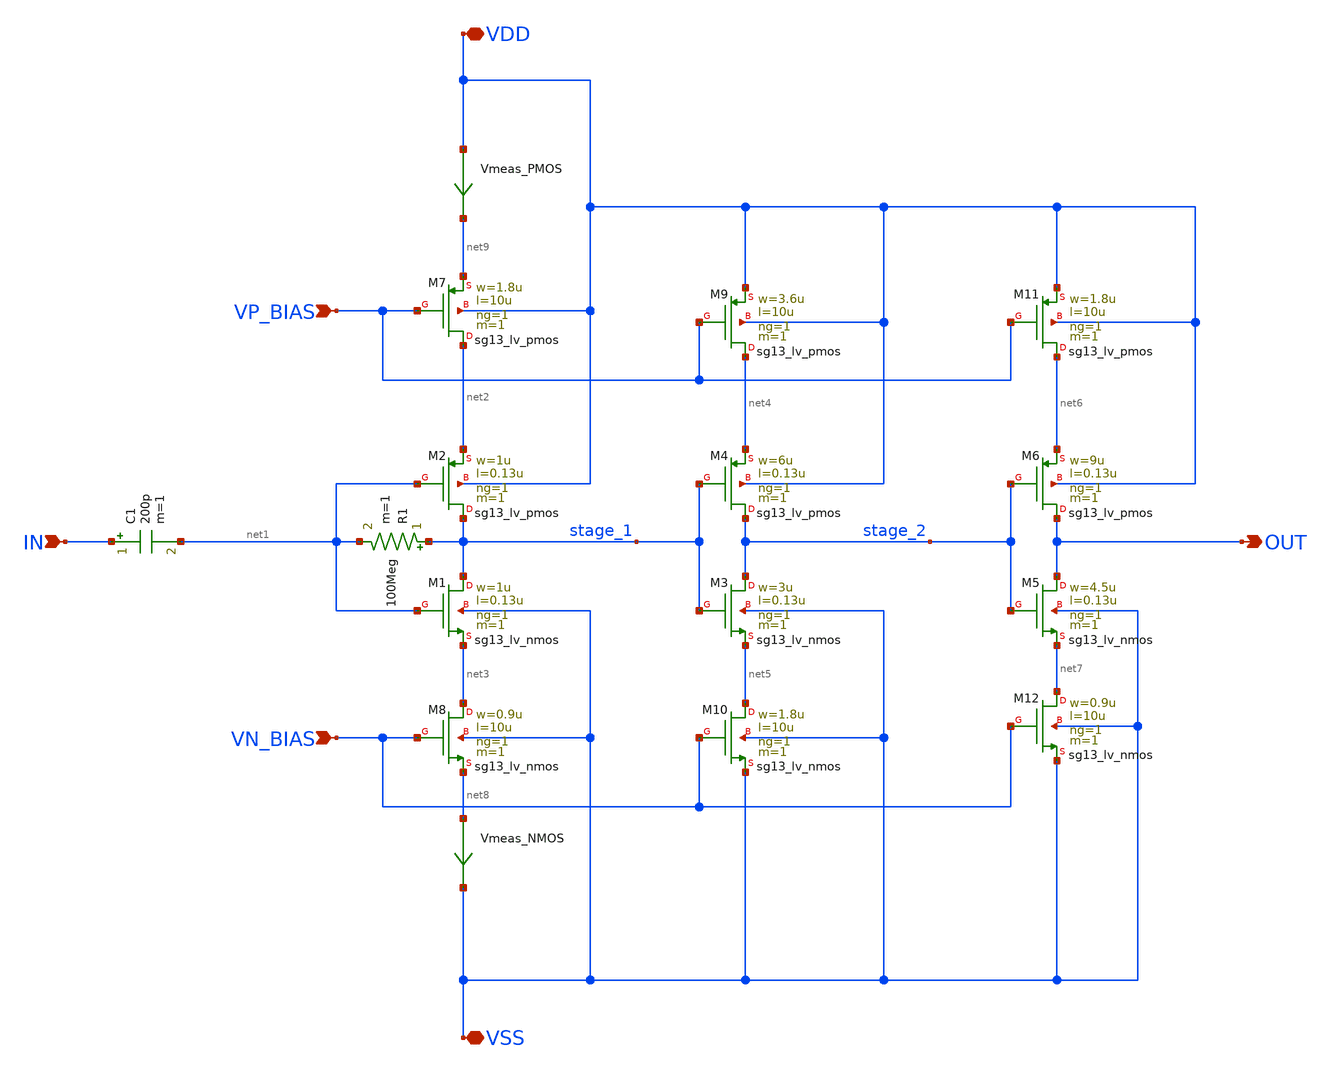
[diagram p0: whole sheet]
** sch_path: clock_gen.sch
**.subckt clock_gen VSS VDD IN OUT VP_BIAS VN_BIAS
*.iopin VSS
*.iopin VDD
*.ipin IN
*.opin OUT
*.ipin VP_BIAS
*.ipin VN_BIAS
XM1 stage_1 net1 net3 VSS sg13_lv_nmos w=1u l=0.13u ng=1 m=1 mm_ok=1
XM2 stage_1 net1 net2 VDD sg13_lv_pmos w=1u l=0.13u ng=1 m=1 mm_ok=1
R1 stage_1 net1 100Meg m=1
C1 IN net1 200p m=1
XM3 stage_2 stage_1 net5 VSS sg13_lv_nmos w=3u l=0.13u ng=1 m=1 mm_ok=1
XM4 stage_2 stage_1 net4 VDD sg13_lv_pmos w=6u l=0.13u ng=1 m=1 mm_ok=1
XM5 OUT stage_2 net7 VSS sg13_lv_nmos w=4.5u l=0.13u ng=1 m=1 mm_ok=1
XM6 OUT stage_2 net6 VDD sg13_lv_pmos w=9u l=0.13u ng=1 m=1 mm_ok=1
XM7 net2 VP_BIAS net9 VDD sg13_lv_pmos w=1.8u l=10u ng=1 m=1 mm_ok=1
XM8 net3 VN_BIAS net8 VSS sg13_lv_nmos w=0.9u l=10u ng=1 m=1 mm_ok=1
XM9 net4 VP_BIAS VDD VDD sg13_lv_pmos w=3.6u l=10u ng=1 m=1 mm_ok=1
XM10 net5 VN_BIAS VSS VSS sg13_lv_nmos w=1.8u l=10u ng=1 m=1 mm_ok=1
XM11 net6 VP_BIAS VDD VDD sg13_lv_pmos w=1.8u l=10u ng=1 m=1 mm_ok=1
XM12 net7 VN_BIAS VSS VSS sg13_lv_nmos w=0.9u l=10u ng=1 m=1 mm_ok=1
Vmeas_NMOS net8 VSS 0
.save i(vmeas_nmos)
Vmeas_PMOS VDD net9 0
.save i(vmeas_pmos)
**.ends
.end
